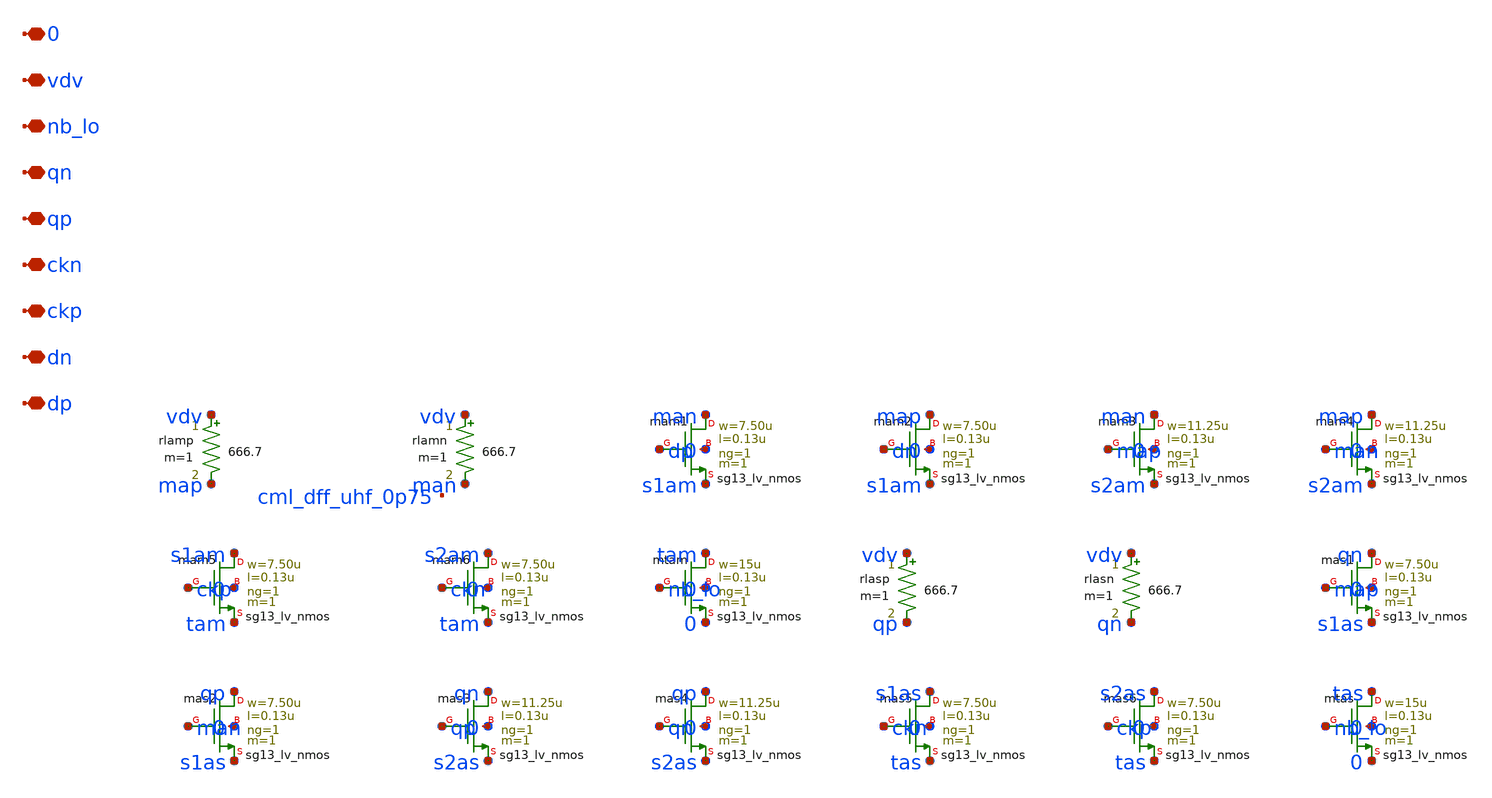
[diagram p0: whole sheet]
** sch_path: analog/lo/sch/cml_dff_uhf.sch
**.subckt cml_dff_uhf dp dn ckp ckn qp qn nb_lo vdv 0
*.iopin dp
*.iopin dn
*.iopin ckp
*.iopin ckn
*.iopin qp
*.iopin qn
*.iopin nb_lo
*.iopin vdv
*.iopin 0
rlamp vdv map 666.7 m=1
rlamn vdv man 666.7 m=1
Xmam1 man dp s1am 0 sg13_lv_nmos w=7.50u l=0.13u ng=1 m=1 mm_ok=1
Xmam2 map dn s1am 0 sg13_lv_nmos w=7.50u l=0.13u ng=1 m=1 mm_ok=1
Xmam3 man map s2am 0 sg13_lv_nmos w=11.25u l=0.13u ng=1 m=1 mm_ok=1
Xmam4 map man s2am 0 sg13_lv_nmos w=11.25u l=0.13u ng=1 m=1 mm_ok=1
Xmam5 s1am ckp tam 0 sg13_lv_nmos w=7.50u l=0.13u ng=1 m=1 mm_ok=1
Xmam6 s2am ckn tam 0 sg13_lv_nmos w=7.50u l=0.13u ng=1 m=1 mm_ok=1
Xmtam tam nb_lo 0 0 sg13_lv_nmos w=15u l=0.13u ng=1 m=1 mm_ok=1
rlasp vdv qp 666.7 m=1
rlasn vdv qn 666.7 m=1
Xmas1 qn map s1as 0 sg13_lv_nmos w=7.50u l=0.13u ng=1 m=1 mm_ok=1
Xmas2 qp man s1as 0 sg13_lv_nmos w=7.50u l=0.13u ng=1 m=1 mm_ok=1
Xmas3 qn qp s2as 0 sg13_lv_nmos w=11.25u l=0.13u ng=1 m=1 mm_ok=1
Xmas4 qp qn s2as 0 sg13_lv_nmos w=11.25u l=0.13u ng=1 m=1 mm_ok=1
Xmas5 s1as ckn tas 0 sg13_lv_nmos w=7.50u l=0.13u ng=1 m=1 mm_ok=1
Xmas6 s2as ckp tas 0 sg13_lv_nmos w=7.50u l=0.13u ng=1 m=1 mm_ok=1
Xmtas tas nb_lo 0 0 sg13_lv_nmos w=15u l=0.13u ng=1 m=1 mm_ok=1
**.ends
.end
